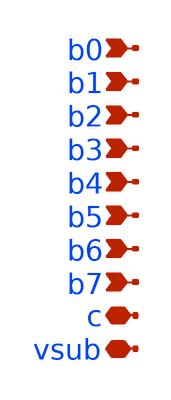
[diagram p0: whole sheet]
** sch_path: xschem/swcap_array_PEX.sch
**.subckt swcap_array_PEX b0 b1 b2 b3 b4 b5 b6 b7 c vsub
*.ipin b0
*.ipin b1
*.ipin b2
*.ipin b3
*.ipin b4
*.ipin b5
*.ipin b6
*.ipin b7
*.iopin c
*.iopin vsub
**** begin user architecture code

.subckt swcap_array C VSUB B0 B1 B2 B3 B4 B5 B6 B7

* NGSPICE file created from swcap_array_1.ext - technology: sky130A

X0 tcap_200f_60/a_173_157# C sky130_fd_pr__cap_mim_m3_2 l=1.6e+06u w=3.14e+07u
X1 tcap_200f_60/a_173_157# B7 VSUB VSUB sky130_fd_pr__nfet_01v8 ad=0p pd=0u as=0p ps=0u w=2e+06u
+ l=150000u
X3 tcap_200f_50/a_173_157# C sky130_fd_pr__cap_mim_m3_2 l=1.6e+06u w=3.14e+07u
X4 tcap_200f_50/a_173_157# B7 VSUB VSUB sky130_fd_pr__nfet_01v8 ad=0p pd=0u as=0p ps=0u w=2e+06u
+ l=150000u
X5 C tcap_200f_50/a_173_157# sky130_fd_pr__cap_mim_m3_1 l=1.6e+06u w=3.14e+07u
X6 tcap_200f_61/a_173_157# C sky130_fd_pr__cap_mim_m3_2 l=1.6e+06u w=3.14e+07u
X7 tcap_200f_61/a_173_157# B7 VSUB VSUB sky130_fd_pr__nfet_01v8 ad=0p pd=0u as=0p ps=0u w=2e+06u
+ l=150000u
X8 C tcap_200f_61/a_173_157# sky130_fd_pr__cap_mim_m3_1 l=1.6e+06u w=3.14e+07u
X9 tcap_200f_40/a_173_157# C sky130_fd_pr__cap_mim_m3_2 l=1.6e+06u w=3.14e+07u
X10 tcap_200f_40/a_173_157# B7 VSUB VSUB sky130_fd_pr__nfet_01v8 ad=0p pd=0u as=0p ps=0u w=2e+06u
+ l=150000u
X11 C tcap_200f_40/a_173_157# sky130_fd_pr__cap_mim_m3_1 l=1.6e+06u w=3.14e+07u
X12 tcap_200f_51/a_173_157# C sky130_fd_pr__cap_mim_m3_2 l=1.6e+06u w=3.14e+07u
X13 tcap_200f_51/a_173_157# B7 VSUB VSUB sky130_fd_pr__nfet_01v8 ad=0p pd=0u as=0p ps=0u w=2e+06u
+ l=150000u
X14 C tcap_200f_51/a_173_157# sky130_fd_pr__cap_mim_m3_1 l=1.6e+06u w=3.14e+07u
X15 tcap_200f_62/a_173_157# C sky130_fd_pr__cap_mim_m3_2 l=1.6e+06u w=3.14e+07u
X16 tcap_200f_62/a_173_157# B7 VSUB VSUB sky130_fd_pr__nfet_01v8 ad=0p pd=0u as=0p ps=0u w=2e+06u
+ l=150000u
X17 C tcap_200f_62/a_173_157# sky130_fd_pr__cap_mim_m3_1 l=1.6e+06u w=3.14e+07u
X18 tcap_200f_30/a_173_157# C sky130_fd_pr__cap_mim_m3_2 l=1.6e+06u w=3.14e+07u
X19 tcap_200f_30/a_173_157# B6 VSUB VSUB sky130_fd_pr__nfet_01v8 ad=0p pd=0u as=0p ps=0u w=2e+06u
+ l=150000u
X20 C tcap_200f_30/a_173_157# sky130_fd_pr__cap_mim_m3_1 l=1.6e+06u w=3.14e+07u
X21 tcap_200f_41/a_173_157# C sky130_fd_pr__cap_mim_m3_2 l=1.6e+06u w=3.14e+07u
X22 tcap_200f_41/a_173_157# B7 VSUB VSUB sky130_fd_pr__nfet_01v8 ad=0p pd=0u as=0p ps=0u w=2e+06u
+ l=150000u
X23 C tcap_200f_41/a_173_157# sky130_fd_pr__cap_mim_m3_1 l=1.6e+06u w=3.14e+07u
X24 tcap_200f_52/a_173_157# C sky130_fd_pr__cap_mim_m3_2 l=1.6e+06u w=3.14e+07u
X25 tcap_200f_52/a_173_157# B7 VSUB VSUB sky130_fd_pr__nfet_01v8 ad=0p pd=0u as=0p ps=0u w=2e+06u
+ l=150000u
X26 C tcap_200f_52/a_173_157# sky130_fd_pr__cap_mim_m3_1 l=1.6e+06u w=3.14e+07u
X27 tcap_200f_63/a_173_157# C sky130_fd_pr__cap_mim_m3_2 l=1.6e+06u w=3.14e+07u
X28 tcap_200f_63/a_173_157# B7 VSUB VSUB sky130_fd_pr__nfet_01v8 ad=0p pd=0u as=0p ps=0u w=2e+06u
+ l=150000u
X29 C tcap_200f_63/a_173_157# sky130_fd_pr__cap_mim_m3_1 l=1.6e+06u w=3.14e+07u
X30 tcap_50f_0/a_173_157# C sky130_fd_pr__cap_mim_m3_2 l=1.6e+06u w=7.85e+06u
X31 tcap_50f_0/a_173_157# B0 VSUB VSUB sky130_fd_pr__nfet_01v8 ad=0p pd=0u as=0p ps=0u w=2e+06u
+ l=150000u
X32 C tcap_50f_0/a_173_157# sky130_fd_pr__cap_mim_m3_1 l=1.6e+06u w=7.85e+06u
X33 tcap_200f_31/a_173_157# C sky130_fd_pr__cap_mim_m3_2 l=1.6e+06u w=3.14e+07u
X34 tcap_200f_31/a_173_157# B6 VSUB VSUB sky130_fd_pr__nfet_01v8 ad=0p pd=0u as=0p ps=0u w=2e+06u
+ l=150000u
X35 C tcap_200f_31/a_173_157# sky130_fd_pr__cap_mim_m3_1 l=1.6e+06u w=3.14e+07u
X36 tcap_200f_42/a_173_157# C sky130_fd_pr__cap_mim_m3_2 l=1.6e+06u w=3.14e+07u
X37 tcap_200f_42/a_173_157# B7 VSUB VSUB sky130_fd_pr__nfet_01v8 ad=0p pd=0u as=0p ps=0u w=2e+06u
+ l=150000u
X38 C tcap_200f_42/a_173_157# sky130_fd_pr__cap_mim_m3_1 l=1.6e+06u w=3.14e+07u
X39 tcap_200f_20/a_173_157# C sky130_fd_pr__cap_mim_m3_2 l=1.6e+06u w=3.14e+07u
X40 tcap_200f_20/a_173_157# B6 VSUB VSUB sky130_fd_pr__nfet_01v8 ad=0p pd=0u as=0p ps=0u w=2e+06u
+ l=150000u
X41 C tcap_200f_20/a_173_157# sky130_fd_pr__cap_mim_m3_1 l=1.6e+06u w=3.14e+07u
X42 tcap_200f_53/a_173_157# C sky130_fd_pr__cap_mim_m3_2 l=1.6e+06u w=3.14e+07u
X43 tcap_200f_53/a_173_157# B7 VSUB VSUB sky130_fd_pr__nfet_01v8 ad=0p pd=0u as=0p ps=0u w=2e+06u
+ l=150000u
X44 C tcap_200f_53/a_173_157# sky130_fd_pr__cap_mim_m3_1 l=1.6e+06u w=3.14e+07u
X45 tcap_200f_64/a_173_157# C sky130_fd_pr__cap_mim_m3_2 l=1.6e+06u w=3.14e+07u
X46 tcap_200f_64/a_173_157# B7 VSUB VSUB sky130_fd_pr__nfet_01v8 ad=0p pd=0u as=0p ps=0u w=2e+06u
+ l=150000u
X47 C tcap_200f_64/a_173_157# sky130_fd_pr__cap_mim_m3_1 l=1.6e+06u w=3.14e+07u
X48 tcap_200f_32/a_173_157# C sky130_fd_pr__cap_mim_m3_2 l=1.6e+06u w=3.14e+07u
X49 tcap_200f_32/a_173_157# B6 VSUB VSUB sky130_fd_pr__nfet_01v8 ad=0p pd=0u as=0p ps=0u w=2e+06u
+ l=150000u
X50 C tcap_200f_32/a_173_157# sky130_fd_pr__cap_mim_m3_1 l=1.6e+06u w=3.14e+07u
X51 tcap_200f_33/a_173_157# C sky130_fd_pr__cap_mim_m3_2 l=1.6e+06u w=3.14e+07u
X52 tcap_200f_33/a_173_157# B7 VSUB VSUB sky130_fd_pr__nfet_01v8 ad=0p pd=0u as=0p ps=0u w=2e+06u
+ l=150000u
X53 C tcap_200f_33/a_173_157# sky130_fd_pr__cap_mim_m3_1 l=1.6e+06u w=3.14e+07u
X54 tcap_200f_43/a_173_157# C sky130_fd_pr__cap_mim_m3_2 l=1.6e+06u w=3.14e+07u
X55 tcap_200f_43/a_173_157# B7 VSUB VSUB sky130_fd_pr__nfet_01v8 ad=0p pd=0u as=0p ps=0u w=2e+06u
+ l=150000u
X56 C tcap_200f_43/a_173_157# sky130_fd_pr__cap_mim_m3_1 l=1.6e+06u w=3.14e+07u
X57 tcap_200f_22/a_173_157# C sky130_fd_pr__cap_mim_m3_2 l=1.6e+06u w=3.14e+07u
X58 tcap_200f_22/a_173_157# B6 VSUB VSUB sky130_fd_pr__nfet_01v8 ad=0p pd=0u as=0p ps=0u w=2e+06u
+ l=150000u
X59 C tcap_200f_22/a_173_157# sky130_fd_pr__cap_mim_m3_1 l=1.6e+06u w=3.14e+07u
X60 tcap_200f_44/a_173_157# C sky130_fd_pr__cap_mim_m3_2 l=1.6e+06u w=3.14e+07u
X61 tcap_200f_44/a_173_157# B7 VSUB VSUB sky130_fd_pr__nfet_01v8 ad=0p pd=0u as=0p ps=0u w=2e+06u
+ l=150000u
X62 C tcap_200f_44/a_173_157# sky130_fd_pr__cap_mim_m3_1 l=1.6e+06u w=3.14e+07u
X63 tcap_200f_21/a_173_157# C sky130_fd_pr__cap_mim_m3_2 l=1.6e+06u w=3.14e+07u
X64 tcap_200f_21/a_173_157# B6 VSUB VSUB sky130_fd_pr__nfet_01v8 ad=0p pd=0u as=0p ps=0u w=2e+06u
+ l=150000u
X65 C tcap_200f_21/a_173_157# sky130_fd_pr__cap_mim_m3_1 l=1.6e+06u w=3.14e+07u
X66 tcap_200f_10/a_173_157# C sky130_fd_pr__cap_mim_m3_2 l=1.6e+06u w=3.14e+07u
X67 tcap_200f_10/a_173_157# B5 VSUB VSUB sky130_fd_pr__nfet_01v8 ad=0p pd=0u as=0p ps=0u w=2e+06u
+ l=150000u
X68 C tcap_200f_10/a_173_157# sky130_fd_pr__cap_mim_m3_1 l=1.6e+06u w=3.14e+07u
X69 tcap_200f_54/a_173_157# C sky130_fd_pr__cap_mim_m3_2 l=1.6e+06u w=3.14e+07u
X70 tcap_200f_54/a_173_157# B7 VSUB VSUB sky130_fd_pr__nfet_01v8 ad=0p pd=0u as=0p ps=0u w=2e+06u
+ l=150000u
X71 C tcap_200f_54/a_173_157# sky130_fd_pr__cap_mim_m3_1 l=1.6e+06u w=3.14e+07u
X72 tcap_200f_11/a_173_157# C sky130_fd_pr__cap_mim_m3_2 l=1.6e+06u w=3.14e+07u
X73 tcap_200f_11/a_173_157# B5 VSUB VSUB sky130_fd_pr__nfet_01v8 ad=0p pd=0u as=0p ps=0u w=2e+06u
+ l=150000u
X74 C tcap_200f_11/a_173_157# sky130_fd_pr__cap_mim_m3_1 l=1.6e+06u w=3.14e+07u
X75 tcap_200f_55/a_173_157# C sky130_fd_pr__cap_mim_m3_2 l=1.6e+06u w=3.14e+07u
X76 tcap_200f_55/a_173_157# B7 VSUB VSUB sky130_fd_pr__nfet_01v8 ad=0p pd=0u as=0p ps=0u w=2e+06u
+ l=150000u
X77 C tcap_200f_55/a_173_157# sky130_fd_pr__cap_mim_m3_1 l=1.6e+06u w=3.14e+07u
X78 tcap_200f_65/a_173_157# C sky130_fd_pr__cap_mim_m3_2 l=1.6e+06u w=3.14e+07u
X79 tcap_200f_65/a_173_157# B7 VSUB VSUB sky130_fd_pr__nfet_01v8 ad=0p pd=0u as=0p ps=0u w=2e+06u
+ l=150000u
X80 C tcap_200f_65/a_173_157# sky130_fd_pr__cap_mim_m3_1 l=1.6e+06u w=3.14e+07u
X81 tcap_200f_34/a_173_157# C sky130_fd_pr__cap_mim_m3_2 l=1.6e+06u w=3.14e+07u
X82 tcap_200f_34/a_173_157# B7 VSUB VSUB sky130_fd_pr__nfet_01v8 ad=0p pd=0u as=0p ps=0u w=2e+06u
+ l=150000u
X83 C tcap_200f_34/a_173_157# sky130_fd_pr__cap_mim_m3_1 l=1.6e+06u w=3.14e+07u
X84 tcap_200f_23/a_173_157# C sky130_fd_pr__cap_mim_m3_2 l=1.6e+06u w=3.14e+07u
X85 tcap_200f_23/a_173_157# B6 VSUB VSUB sky130_fd_pr__nfet_01v8 ad=0p pd=0u as=0p ps=0u w=2e+06u
+ l=150000u
X86 C tcap_200f_23/a_173_157# sky130_fd_pr__cap_mim_m3_1 l=1.6e+06u w=3.14e+07u
X87 tcap_200f_45/a_173_157# C sky130_fd_pr__cap_mim_m3_2 l=1.6e+06u w=3.14e+07u
X88 tcap_200f_45/a_173_157# B7 VSUB VSUB sky130_fd_pr__nfet_01v8 ad=0p pd=0u as=0p ps=0u w=2e+06u
+ l=150000u
X89 C tcap_200f_45/a_173_157# sky130_fd_pr__cap_mim_m3_1 l=1.6e+06u w=3.14e+07u
X90 tcap_200f_12/a_173_157# C sky130_fd_pr__cap_mim_m3_2 l=1.6e+06u w=3.14e+07u
X91 tcap_200f_12/a_173_157# B5 VSUB VSUB sky130_fd_pr__nfet_01v8 ad=0p pd=0u as=0p ps=0u w=2e+06u
+ l=150000u
X92 C tcap_200f_12/a_173_157# sky130_fd_pr__cap_mim_m3_1 l=1.6e+06u w=3.14e+07u
X93 tcap_200f_0/a_173_157# C sky130_fd_pr__cap_mim_m3_2 l=1.6e+06u w=3.14e+07u
X94 tcap_200f_0/a_173_157# B5 VSUB VSUB sky130_fd_pr__nfet_01v8 ad=0p pd=0u as=0p ps=0u w=2e+06u
+ l=150000u
X95 C tcap_200f_0/a_173_157# sky130_fd_pr__cap_mim_m3_1 l=1.6e+06u w=3.14e+07u
X96 tcap_200f_56/a_173_157# C sky130_fd_pr__cap_mim_m3_2 l=1.6e+06u w=3.14e+07u
X97 tcap_200f_56/a_173_157# B7 VSUB VSUB sky130_fd_pr__nfet_01v8 ad=0p pd=0u as=0p ps=0u w=2e+06u
+ l=150000u
X98 C tcap_200f_56/a_173_157# sky130_fd_pr__cap_mim_m3_1 l=1.6e+06u w=3.14e+07u
X99 tcap_200f_35/a_173_157# C sky130_fd_pr__cap_mim_m3_2 l=1.6e+06u w=3.14e+07u
X100 tcap_200f_35/a_173_157# B7 VSUB VSUB sky130_fd_pr__nfet_01v8 ad=0p pd=0u as=0p ps=0u w=2e+06u
+ l=150000u
X101 C tcap_200f_35/a_173_157# sky130_fd_pr__cap_mim_m3_1 l=1.6e+06u w=3.14e+07u
X102 tcap_200f_24/a_173_157# C sky130_fd_pr__cap_mim_m3_2 l=1.6e+06u w=3.14e+07u
X103 tcap_200f_24/a_173_157# B6 VSUB VSUB sky130_fd_pr__nfet_01v8 ad=0p pd=0u as=0p ps=0u w=2e+06u
+ l=150000u
X104 C tcap_200f_24/a_173_157# sky130_fd_pr__cap_mim_m3_1 l=1.6e+06u w=3.14e+07u
X105 tcap_200f_46/a_173_157# C sky130_fd_pr__cap_mim_m3_2 l=1.6e+06u w=3.14e+07u
X106 tcap_200f_46/a_173_157# B7 VSUB VSUB sky130_fd_pr__nfet_01v8 ad=0p pd=0u as=0p ps=0u w=2e+06u
+ l=150000u
X107 C tcap_200f_46/a_173_157# sky130_fd_pr__cap_mim_m3_1 l=1.6e+06u w=3.14e+07u
X108 tcap_200f_13/a_173_157# C sky130_fd_pr__cap_mim_m3_2 l=1.6e+06u w=3.14e+07u
X109 tcap_200f_13/a_173_157# B5 VSUB VSUB sky130_fd_pr__nfet_01v8 ad=0p pd=0u as=0p ps=0u w=2e+06u
+ l=150000u
X110 C tcap_200f_13/a_173_157# sky130_fd_pr__cap_mim_m3_1 l=1.6e+06u w=3.14e+07u
X111 tcap_200f_57/a_173_157# C sky130_fd_pr__cap_mim_m3_2 l=1.6e+06u w=3.14e+07u
X112 tcap_200f_57/a_173_157# B7 VSUB VSUB sky130_fd_pr__nfet_01v8 ad=0p pd=0u as=0p ps=0u w=2e+06u
+ l=150000u
X113 C tcap_200f_57/a_173_157# sky130_fd_pr__cap_mim_m3_1 l=1.6e+06u w=3.14e+07u
X114 tcap_200f_36/a_173_157# C sky130_fd_pr__cap_mim_m3_2 l=1.6e+06u w=3.14e+07u
X115 tcap_200f_36/a_173_157# B7 VSUB VSUB sky130_fd_pr__nfet_01v8 ad=0p pd=0u as=0p ps=0u w=2e+06u
+ l=150000u
X116 C tcap_200f_36/a_173_157# sky130_fd_pr__cap_mim_m3_1 l=1.6e+06u w=3.14e+07u
X117 tcap_200f_25/a_173_157# C sky130_fd_pr__cap_mim_m3_2 l=1.6e+06u w=3.14e+07u
X118 tcap_200f_25/a_173_157# B6 VSUB VSUB sky130_fd_pr__nfet_01v8 ad=0p pd=0u as=0p ps=0u w=2e+06u
+ l=150000u
X119 C tcap_200f_25/a_173_157# sky130_fd_pr__cap_mim_m3_1 l=1.6e+06u w=3.14e+07u
X120 tcap_200f_47/a_173_157# C sky130_fd_pr__cap_mim_m3_2 l=1.6e+06u w=3.14e+07u
X121 tcap_200f_47/a_173_157# B7 VSUB VSUB sky130_fd_pr__nfet_01v8 ad=0p pd=0u as=0p ps=0u w=2e+06u
+ l=150000u
X122 C tcap_200f_47/a_173_157# sky130_fd_pr__cap_mim_m3_1 l=1.6e+06u w=3.14e+07u
X123 tcap_200f_14/a_173_157# C sky130_fd_pr__cap_mim_m3_2 l=1.6e+06u w=3.14e+07u
X124 tcap_200f_14/a_173_157# B5 VSUB VSUB sky130_fd_pr__nfet_01v8 ad=0p pd=0u as=0p ps=0u w=2e+06u
+ l=150000u
X125 C tcap_200f_14/a_173_157# sky130_fd_pr__cap_mim_m3_1 l=1.6e+06u w=3.14e+07u
X126 tcap_200f_58/a_173_157# C sky130_fd_pr__cap_mim_m3_2 l=1.6e+06u w=3.14e+07u
X127 tcap_200f_58/a_173_157# B7 VSUB VSUB sky130_fd_pr__nfet_01v8 ad=0p pd=0u as=0p ps=0u w=2e+06u
+ l=150000u
X128 C tcap_200f_58/a_173_157# sky130_fd_pr__cap_mim_m3_1 l=1.6e+06u w=3.14e+07u
X129 tcap_200f_37/a_173_157# C sky130_fd_pr__cap_mim_m3_2 l=1.6e+06u w=3.14e+07u
X130 tcap_200f_37/a_173_157# B7 VSUB VSUB sky130_fd_pr__nfet_01v8 ad=0p pd=0u as=0p ps=0u w=2e+06u
+ l=150000u
X131 C tcap_200f_37/a_173_157# sky130_fd_pr__cap_mim_m3_1 l=1.6e+06u w=3.14e+07u
X132 tcap_200f_26/a_173_157# C sky130_fd_pr__cap_mim_m3_2 l=1.6e+06u w=3.14e+07u
X133 tcap_200f_26/a_173_157# B6 VSUB VSUB sky130_fd_pr__nfet_01v8 ad=0p pd=0u as=0p ps=0u w=2e+06u
+ l=150000u
X134 C tcap_200f_26/a_173_157# sky130_fd_pr__cap_mim_m3_1 l=1.6e+06u w=3.14e+07u
X135 tcap_200f_15/a_173_157# C sky130_fd_pr__cap_mim_m3_2 l=1.6e+06u w=3.14e+07u
X136 tcap_200f_15/a_173_157# B6 VSUB VSUB sky130_fd_pr__nfet_01v8 ad=0p pd=0u as=0p ps=0u w=2e+06u
+ l=150000u
X137 C tcap_200f_15/a_173_157# sky130_fd_pr__cap_mim_m3_1 l=1.6e+06u w=3.14e+07u
X138 tcap_200f_48/a_173_157# C sky130_fd_pr__cap_mim_m3_2 l=1.6e+06u w=3.14e+07u
X139 tcap_200f_48/a_173_157# B7 VSUB VSUB sky130_fd_pr__nfet_01v8 ad=0p pd=0u as=0p ps=0u w=2e+06u
+ l=150000u
X140 C tcap_200f_48/a_173_157# sky130_fd_pr__cap_mim_m3_1 l=1.6e+06u w=3.14e+07u
X141 tcap_200f_59/a_173_157# C sky130_fd_pr__cap_mim_m3_2 l=1.6e+06u w=3.14e+07u
X142 tcap_200f_59/a_173_157# B7 VSUB VSUB sky130_fd_pr__nfet_01v8 ad=0p pd=0u as=0p ps=0u w=2e+06u
+ l=150000u
X143 C tcap_200f_59/a_173_157# sky130_fd_pr__cap_mim_m3_1 l=1.6e+06u w=3.14e+07u
X144 tcap_200f_3/a_173_157# C sky130_fd_pr__cap_mim_m3_2 l=1.6e+06u w=3.14e+07u
X145 tcap_200f_3/a_173_157# B2 VSUB VSUB sky130_fd_pr__nfet_01v8 ad=0p pd=0u as=0p ps=0u w=2e+06u
+ l=150000u
X146 C tcap_200f_3/a_173_157# sky130_fd_pr__cap_mim_m3_1 l=1.6e+06u w=3.14e+07u
X147 tcap_200f_38/a_173_157# C sky130_fd_pr__cap_mim_m3_2 l=1.6e+06u w=3.14e+07u
X148 tcap_200f_38/a_173_157# B7 VSUB VSUB sky130_fd_pr__nfet_01v8 ad=0p pd=0u as=0p ps=0u w=2e+06u
+ l=150000u
X149 C tcap_200f_38/a_173_157# sky130_fd_pr__cap_mim_m3_1 l=1.6e+06u w=3.14e+07u
X150 tcap_200f_27/a_173_157# C sky130_fd_pr__cap_mim_m3_2 l=1.6e+06u w=3.14e+07u
X151 tcap_200f_27/a_173_157# B6 VSUB VSUB sky130_fd_pr__nfet_01v8 ad=0p pd=0u as=0p ps=0u w=2e+06u
+ l=150000u
X152 C tcap_200f_27/a_173_157# sky130_fd_pr__cap_mim_m3_1 l=1.6e+06u w=3.14e+07u
X153 tcap_200f_16/a_173_157# C sky130_fd_pr__cap_mim_m3_2 l=1.6e+06u w=3.14e+07u
X154 tcap_200f_16/a_173_157# B5 VSUB VSUB sky130_fd_pr__nfet_01v8 ad=0p pd=0u as=0p ps=0u w=2e+06u
+ l=150000u
X155 C tcap_200f_16/a_173_157# sky130_fd_pr__cap_mim_m3_1 l=1.6e+06u w=3.14e+07u
X156 tcap_200f_49/a_173_157# C sky130_fd_pr__cap_mim_m3_2 l=1.6e+06u w=3.14e+07u
X157 tcap_200f_49/a_173_157# B7 VSUB VSUB sky130_fd_pr__nfet_01v8 ad=0p pd=0u as=0p ps=0u w=2e+06u
+ l=150000u
X158 C tcap_200f_49/a_173_157# sky130_fd_pr__cap_mim_m3_1 l=1.6e+06u w=3.14e+07u
X159 tcap_200f_4/a_173_157# C sky130_fd_pr__cap_mim_m3_2 l=1.6e+06u w=3.14e+07u
X160 tcap_200f_4/a_173_157# B3 VSUB VSUB sky130_fd_pr__nfet_01v8 ad=0p pd=0u as=0p ps=0u w=2e+06u
+ l=150000u
X161 C tcap_200f_4/a_173_157# sky130_fd_pr__cap_mim_m3_1 l=1.6e+06u w=3.14e+07u
X162 tcap_200f_28/a_173_157# C sky130_fd_pr__cap_mim_m3_2 l=1.6e+06u w=3.14e+07u
X163 tcap_200f_28/a_173_157# B6 VSUB VSUB sky130_fd_pr__nfet_01v8 ad=0p pd=0u as=0p ps=0u w=2e+06u
+ l=150000u
X164 C tcap_200f_28/a_173_157# sky130_fd_pr__cap_mim_m3_1 l=1.6e+06u w=3.14e+07u
X165 tcap_200f_39/a_173_157# C sky130_fd_pr__cap_mim_m3_2 l=1.6e+06u w=3.14e+07u
X166 tcap_200f_39/a_173_157# B7 VSUB VSUB sky130_fd_pr__nfet_01v8 ad=0p pd=0u as=0p ps=0u w=2e+06u
+ l=150000u
X167 C tcap_200f_39/a_173_157# sky130_fd_pr__cap_mim_m3_1 l=1.6e+06u w=3.14e+07u
X168 tcap_200f_17/a_173_157# C sky130_fd_pr__cap_mim_m3_2 l=1.6e+06u w=3.14e+07u
X169 tcap_200f_17/a_173_157# B5 VSUB VSUB sky130_fd_pr__nfet_01v8 ad=0p pd=0u as=0p ps=0u w=2e+06u
+ l=150000u
X170 C tcap_200f_17/a_173_157# sky130_fd_pr__cap_mim_m3_1 l=1.6e+06u w=3.14e+07u
X171 tcap_200f_5/a_173_157# C sky130_fd_pr__cap_mim_m3_2 l=1.6e+06u w=3.14e+07u
X172 tcap_200f_5/a_173_157# B3 VSUB VSUB sky130_fd_pr__nfet_01v8 ad=0p pd=0u as=0p ps=0u w=2e+06u
+ l=150000u
X173 C tcap_200f_5/a_173_157# sky130_fd_pr__cap_mim_m3_1 l=1.6e+06u w=3.14e+07u
X174 tcap_200f_29/a_173_157# C sky130_fd_pr__cap_mim_m3_2 l=1.6e+06u w=3.14e+07u
X175 tcap_200f_29/a_173_157# B6 VSUB VSUB sky130_fd_pr__nfet_01v8 ad=0p pd=0u as=0p ps=0u w=2e+06u
+ l=150000u
X176 C tcap_200f_29/a_173_157# sky130_fd_pr__cap_mim_m3_1 l=1.6e+06u w=3.14e+07u
X177 tcap_200f_18/a_173_157# C sky130_fd_pr__cap_mim_m3_2 l=1.6e+06u w=3.14e+07u
X178 tcap_200f_18/a_173_157# B6 VSUB VSUB sky130_fd_pr__nfet_01v8 ad=0p pd=0u as=0p ps=0u w=2e+06u
+ l=150000u
X179 C tcap_200f_18/a_173_157# sky130_fd_pr__cap_mim_m3_1 l=1.6e+06u w=3.14e+07u
X180 tcap_200f_6/a_173_157# C sky130_fd_pr__cap_mim_m3_2 l=1.6e+06u w=3.14e+07u
X181 tcap_200f_6/a_173_157# B4 VSUB VSUB sky130_fd_pr__nfet_01v8 ad=0p pd=0u as=0p ps=0u w=2e+06u
+ l=150000u
X182 C tcap_200f_6/a_173_157# sky130_fd_pr__cap_mim_m3_1 l=1.6e+06u w=3.14e+07u
X183 tcap_200f_19/a_173_157# C sky130_fd_pr__cap_mim_m3_2 l=1.6e+06u w=3.14e+07u
X184 tcap_200f_19/a_173_157# B6 VSUB VSUB sky130_fd_pr__nfet_01v8 ad=0p pd=0u as=0p ps=0u w=2e+06u
+ l=150000u
X185 C tcap_200f_19/a_173_157# sky130_fd_pr__cap_mim_m3_1 l=1.6e+06u w=3.14e+07u
X186 tcap_200f_8/a_173_157# C sky130_fd_pr__cap_mim_m3_2 l=1.6e+06u w=3.14e+07u
X187 tcap_200f_8/a_173_157# B4 VSUB VSUB sky130_fd_pr__nfet_01v8 ad=0p pd=0u as=0p ps=0u w=2e+06u
+ l=150000u
X188 C tcap_200f_8/a_173_157# sky130_fd_pr__cap_mim_m3_1 l=1.6e+06u w=3.14e+07u
X189 tcap_200f_7/a_173_157# C sky130_fd_pr__cap_mim_m3_2 l=1.6e+06u w=3.14e+07u
X190 tcap_200f_7/a_173_157# B4 VSUB VSUB sky130_fd_pr__nfet_01v8 ad=0p pd=0u as=0p ps=0u w=2e+06u
+ l=150000u
X191 C tcap_200f_7/a_173_157# sky130_fd_pr__cap_mim_m3_1 l=1.6e+06u w=3.14e+07u
X192 tcap_200f_9/a_173_157# C sky130_fd_pr__cap_mim_m3_2 l=1.6e+06u w=3.14e+07u
X193 tcap_200f_9/a_173_157# B4 VSUB VSUB sky130_fd_pr__nfet_01v8 ad=0p pd=0u as=0p ps=0u w=2e+06u
+ l=150000u
X194 C tcap_200f_9/a_173_157# sky130_fd_pr__cap_mim_m3_1 l=1.6e+06u w=3.14e+07u
X195 tcap_100f_0/a_173_157# C sky130_fd_pr__cap_mim_m3_2 l=1.6e+06u w=1.57e+07u
X196 tcap_100f_0/a_173_157# B1 VSUB VSUB sky130_fd_pr__nfet_01v8 ad=0p pd=0u as=0p ps=0u w=2e+06u
+ l=150000u
X197 C tcap_100f_0/a_173_157# sky130_fd_pr__cap_mim_m3_1 l=1.6e+06u w=1.57e+07u
C0 C tcap_100f_0/a_173_157# 5.85fF
C1 tcap_200f_36/a_173_157# tcap_200f_37/a_173_157# 4.48fF
C2 tcap_200f_38/a_173_157# tcap_200f_37/a_173_157# 4.48fF
C3 tcap_200f_28/a_173_157# tcap_200f_31/a_173_157# 4.47fF
C4 tcap_200f_10/a_173_157# tcap_200f_13/a_173_157# 4.47fF
C5 tcap_200f_45/a_173_157# C 12.05fF
C6 tcap_200f_44/a_173_157# C 12.05fF
C7 tcap_200f_16/a_173_157# tcap_200f_14/a_173_157# 4.47fF
C8 C tcap_200f_52/a_173_157# 12.05fF
C9 tcap_200f_57/a_173_157# tcap_200f_58/a_173_157# 4.48fF
C10 tcap_200f_17/a_173_157# tcap_200f_16/a_173_157# 4.47fF
C11 tcap_200f_18/a_173_157# C 12.05fF
C12 tcap_200f_12/a_173_157# C 12.05fF
C13 tcap_200f_47/a_173_157# tcap_200f_46/a_173_157# 4.48fF
C14 tcap_200f_49/a_173_157# tcap_200f_50/a_173_157# 4.48fF
C15 tcap_200f_56/a_173_157# C 12.05fF
C16 tcap_200f_54/a_173_157# tcap_200f_53/a_173_157# 4.48fF
C17 tcap_200f_41/a_173_157# tcap_200f_40/a_173_157# 4.48fF
C18 tcap_200f_15/a_173_157# C 12.05fF
C19 C tcap_200f_7/a_173_157# 12.05fF
C20 tcap_200f_15/a_173_157# tcap_200f_25/a_173_157# 4.47fF
C21 tcap_200f_36/a_173_157# C 12.05fF
C22 tcap_200f_38/a_173_157# C 12.05fF
C23 tcap_200f_5/a_173_157# C 12.05fF
C24 tcap_200f_22/a_173_157# C 12.05fF
C25 tcap_200f_42/a_173_157# C 12.05fF
C26 tcap_200f_48/a_173_157# tcap_200f_47/a_173_157# 4.48fF
C27 tcap_200f_34/a_173_157# C 11.79fF
C28 tcap_200f_52/a_173_157# tcap_200f_53/a_173_157# 4.48fF
C29 C tcap_200f_6/a_173_157# 12.05fF
C30 tcap_200f_44/a_173_157# tcap_200f_43/a_173_157# 4.48fF
C31 tcap_200f_31/a_173_157# tcap_200f_30/a_173_157# 4.47fF
C32 tcap_200f_36/a_173_157# tcap_200f_35/a_173_157# 4.48fF
C33 tcap_200f_39/a_173_157# C 12.05fF
C34 tcap_200f_45/a_173_157# tcap_200f_46/a_173_157# 4.48fF
C35 tcap_200f_4/a_173_157# tcap_200f_3/a_173_157# 4.47fF
C36 tcap_200f_16/a_173_157# C 12.05fF
C37 tcap_200f_59/a_173_157# C 12.05fF
C38 tcap_200f_14/a_173_157# C 12.05fF
C39 tcap_200f_23/a_173_157# tcap_200f_22/a_173_157# 4.47fF
C40 tcap_200f_34/a_173_157# tcap_200f_35/a_173_157# 4.48fF
C41 tcap_200f_61/a_173_157# tcap_200f_62/a_173_157# 4.48fF
C42 tcap_200f_55/a_173_157# tcap_200f_54/a_173_157# 4.48fF
C43 C tcap_200f_37/a_173_157# 12.05fF
C44 tcap_200f_15/a_173_157# tcap_200f_27/a_173_157# 4.47fF
C45 tcap_200f_51/a_173_157# tcap_200f_50/a_173_157# 4.48fF
C46 tcap_200f_63/a_173_157# tcap_200f_62/a_173_157# 4.48fF
C47 tcap_200f_57/a_173_157# tcap_200f_56/a_173_157# 4.48fF
C48 tcap_200f_17/a_173_157# C 12.05fF
C49 tcap_200f_11/a_173_157# tcap_200f_0/a_173_157# 4.47fF
C50 tcap_50f_0/a_173_157# C 3.01fF
C51 tcap_200f_8/a_173_157# tcap_200f_7/a_173_157# 4.47fF
C52 tcap_200f_11/a_173_157# C 12.05fF
C53 tcap_200f_42/a_173_157# tcap_200f_43/a_173_157# 4.48fF
C54 tcap_200f_60/a_173_157# tcap_200f_61/a_173_157# 4.48fF
C55 tcap_200f_3/a_173_157# tcap_100f_0/a_173_157# 2.53fF
C56 tcap_200f_21/a_173_157# tcap_200f_22/a_173_157# 4.47fF
C57 tcap_200f_0/a_173_157# C 12.05fF
C58 tcap_200f_24/a_173_157# C 12.05fF
C59 tcap_200f_52/a_173_157# tcap_200f_51/a_173_157# 4.48fF
C60 tcap_200f_55/a_173_157# tcap_200f_56/a_173_157# 4.48fF
C61 tcap_200f_24/a_173_157# tcap_200f_25/a_173_157# 4.47fF
C62 tcap_200f_64/a_173_157# C 11.71fF
C63 tcap_200f_29/a_173_157# C 12.05fF
C64 B4 B5 3.35fF
C65 tcap_200f_20/a_173_157# C 12.05fF
C66 tcap_200f_42/a_173_157# tcap_200f_41/a_173_157# 4.48fF
C67 tcap_200f_25/a_173_157# C 12.05fF
C68 tcap_200f_18/a_173_157# tcap_200f_19/a_173_157# 4.47fF
C69 tcap_200f_23/a_173_157# tcap_200f_24/a_173_157# 4.47fF
C70 tcap_200f_10/a_173_157# tcap_200f_11/a_173_157# 4.47fF
C71 tcap_200f_12/a_173_157# tcap_200f_13/a_173_157# 4.47fF
C72 C tcap_200f_35/a_173_157# 12.05fF
C73 tcap_200f_5/a_173_157# tcap_200f_4/a_173_157# 4.47fF
C74 B5 B6 6.53fF
C75 tcap_200f_29/a_173_157# tcap_200f_28/a_173_157# 4.47fF
C76 tcap_200f_23/a_173_157# C 12.05fF
C77 tcap_200f_26/a_173_157# tcap_200f_29/a_173_157# 4.47fF
C78 tcap_200f_28/a_173_157# C 12.05fF
C79 tcap_200f_44/a_173_157# tcap_200f_45/a_173_157# 4.48fF
C80 tcap_200f_26/a_173_157# C 12.05fF
C81 tcap_200f_9/a_173_157# tcap_200f_0/a_173_157# 4.47fF
C82 tcap_200f_32/a_173_157# C 11.60fF
C83 tcap_200f_10/a_173_157# C 12.05fF
C84 tcap_200f_27/a_173_157# C 12.05fF
C85 tcap_200f_39/a_173_157# tcap_200f_40/a_173_157# 4.48fF
C86 tcap_200f_34/a_173_157# tcap_200f_33/a_173_157# 4.48fF
C87 C tcap_200f_53/a_173_157# 12.05fF
C88 tcap_200f_57/a_173_157# C 12.05fF
C89 tcap_200f_43/a_173_157# C 12.05fF
C90 tcap_200f_9/a_173_157# C 12.05fF
C91 tcap_200f_49/a_173_157# C 12.05fF
C92 C tcap_200f_8/a_173_157# 12.05fF
C93 C tcap_200f_46/a_173_157# 12.05fF
C94 tcap_200f_21/a_173_157# C 12.05fF
C95 tcap_200f_21/a_173_157# tcap_200f_20/a_173_157# 4.47fF
C96 tcap_200f_59/a_173_157# tcap_200f_58/a_173_157# 4.48fF
C97 tcap_200f_64/a_173_157# tcap_200f_65/a_173_157# 4.48fF
C98 C tcap_200f_65/a_173_157# 10.91fF
C99 tcap_200f_41/a_173_157# C 12.05fF
C100 tcap_200f_26/a_173_157# tcap_200f_27/a_173_157# 4.47fF
C101 tcap_200f_48/a_173_157# C 12.05fF
C102 tcap_200f_55/a_173_157# C 12.05fF
C103 tcap_200f_59/a_173_157# tcap_200f_60/a_173_157# 4.48fF
C104 C tcap_200f_30/a_173_157# 11.79fF
C105 tcap_200f_4/a_173_157# C 11.89fF
C106 B7 B6 9.55fF
C107 C tcap_200f_62/a_173_157# 12.05fF
C108 C tcap_200f_51/a_173_157# 12.05fF
C109 tcap_200f_19/a_173_157# C 12.05fF
C110 tcap_200f_19/a_173_157# tcap_200f_20/a_173_157# 4.47fF
C111 tcap_200f_9/a_173_157# tcap_200f_8/a_173_157# 4.47fF
C112 C tcap_200f_40/a_173_157# 12.05fF
C113 C tcap_200f_13/a_173_157# 12.05fF
C114 tcap_200f_6/a_173_157# tcap_200f_7/a_173_157# 4.47fF
C115 C tcap_200f_3/a_173_157# 11.41fF
C116 tcap_200f_33/a_173_157# C 11.60fF
C117 tcap_200f_61/a_173_157# C 12.05fF
C118 tcap_200f_14/a_173_157# tcap_200f_12/a_173_157# 4.47fF
C119 tcap_200f_47/a_173_157# C 12.05fF
C120 tcap_200f_58/a_173_157# C 12.05fF
C121 C tcap_200f_31/a_173_157# 12.05fF
C122 tcap_200f_64/a_173_157# tcap_200f_63/a_173_157# 4.48fF
C123 tcap_200f_5/a_173_157# tcap_200f_6/a_173_157# 4.47fF
C124 tcap_200f_32/a_173_157# tcap_200f_30/a_173_157# 4.47fF
C125 C tcap_200f_50/a_173_157# 12.05fF
C126 tcap_200f_39/a_173_157# tcap_200f_38/a_173_157# 4.48fF
C127 C tcap_200f_63/a_173_157# 12.04fF
C128 tcap_200f_18/a_173_157# tcap_200f_17/a_173_157# 4.47fF
C129 tcap_200f_48/a_173_157# tcap_200f_49/a_173_157# 4.48fF
C130 tcap_200f_60/a_173_157# C 12.05fF
C131 tcap_200f_54/a_173_157# C 12.05fF
C132 tcap_100f_0/a_173_157# VSUB 4.99fF $ **FLOATING
C133 tcap_200f_9/a_173_157# VSUB 7.94fF $ **FLOATING
C134 tcap_200f_7/a_173_157# VSUB 7.94fF $ **FLOATING
C135 tcap_200f_8/a_173_157# VSUB 7.94fF $ **FLOATING
C136 tcap_200f_19/a_173_157# VSUB 7.94fF $ **FLOATING
C137 tcap_200f_6/a_173_157# VSUB 7.94fF $ **FLOATING
C138 B4 VSUB 5.01fF $ **FLOATING
C139 tcap_200f_18/a_173_157# VSUB 7.94fF $ **FLOATING
C140 B6 VSUB 22.15fF $ **FLOATING
C141 tcap_200f_29/a_173_157# VSUB 7.94fF $ **FLOATING
C142 tcap_200f_5/a_173_157# VSUB 7.94fF $ **FLOATING
C143 tcap_200f_17/a_173_157# VSUB 7.94fF $ **FLOATING
C144 tcap_200f_39/a_173_157# VSUB 7.96fF $ **FLOATING
C145 tcap_200f_28/a_173_157# VSUB 7.94fF $ **FLOATING
C146 tcap_200f_4/a_173_157# VSUB 7.94fF $ **FLOATING
C147 B3 VSUB 2.41fF $ **FLOATING
C148 tcap_200f_49/a_173_157# VSUB 7.96fF $ **FLOATING
C149 tcap_200f_16/a_173_157# VSUB 7.94fF $ **FLOATING
C150 tcap_200f_27/a_173_157# VSUB 7.94fF $ **FLOATING
C151 tcap_200f_38/a_173_157# VSUB 7.96fF $ **FLOATING
C152 tcap_200f_3/a_173_157# VSUB 7.94fF $ **FLOATING
C153 tcap_200f_59/a_173_157# VSUB 7.95fF $ **FLOATING
C154 tcap_200f_48/a_173_157# VSUB 7.96fF $ **FLOATING
C155 tcap_200f_15/a_173_157# VSUB 7.94fF $ **FLOATING
C156 tcap_200f_26/a_173_157# VSUB 7.94fF $ **FLOATING
C157 tcap_200f_37/a_173_157# VSUB 7.96fF $ **FLOATING
C158 tcap_200f_58/a_173_157# VSUB 7.95fF $ **FLOATING
C159 tcap_200f_14/a_173_157# VSUB 7.94fF $ **FLOATING
C160 tcap_200f_47/a_173_157# VSUB 7.96fF $ **FLOATING
C161 tcap_200f_25/a_173_157# VSUB 7.94fF $ **FLOATING
C162 tcap_200f_36/a_173_157# VSUB 7.96fF $ **FLOATING
C163 tcap_200f_57/a_173_157# VSUB 7.95fF $ **FLOATING
C164 tcap_200f_13/a_173_157# VSUB 7.94fF $ **FLOATING
C165 tcap_200f_46/a_173_157# VSUB 7.96fF $ **FLOATING
C166 tcap_200f_24/a_173_157# VSUB 7.94fF $ **FLOATING
C167 tcap_200f_35/a_173_157# VSUB 7.96fF $ **FLOATING
C168 tcap_200f_56/a_173_157# VSUB 7.95fF $ **FLOATING
C169 tcap_200f_0/a_173_157# VSUB 7.94fF $ **FLOATING
C170 B5 VSUB 10.51fF $ **FLOATING
C171 tcap_200f_12/a_173_157# VSUB 7.94fF $ **FLOATING
C172 tcap_200f_45/a_173_157# VSUB 7.96fF $ **FLOATING
C173 tcap_200f_23/a_173_157# VSUB 7.94fF $ **FLOATING
C174 tcap_200f_34/a_173_157# VSUB 7.95fF $ **FLOATING
C175 C VSUB 71.74fF $ **FLOATING
C176 tcap_200f_65/a_173_157# VSUB 7.92fF $ **FLOATING
C177 B7 VSUB 28.92fF $ **FLOATING
C178 tcap_200f_55/a_173_157# VSUB 7.95fF $ **FLOATING
C179 tcap_200f_11/a_173_157# VSUB 7.94fF $ **FLOATING
C180 tcap_200f_54/a_173_157# VSUB 7.95fF $ **FLOATING
C181 tcap_200f_10/a_173_157# VSUB 7.94fF $ **FLOATING
C182 tcap_200f_21/a_173_157# VSUB 7.94fF $ **FLOATING
C183 tcap_200f_44/a_173_157# VSUB 7.96fF $ **FLOATING
C184 tcap_200f_22/a_173_157# VSUB 7.94fF $ **FLOATING
C185 tcap_200f_43/a_173_157# VSUB 7.96fF $ **FLOATING
C186 tcap_200f_33/a_173_157# VSUB 7.96fF $ **FLOATING
C187 tcap_200f_32/a_173_157# VSUB 7.96fF $ **FLOATING
C188 tcap_200f_64/a_173_157# VSUB 7.93fF $ **FLOATING
C189 tcap_200f_53/a_173_157# VSUB 7.95fF $ **FLOATING
C190 tcap_200f_20/a_173_157# VSUB 7.94fF $ **FLOATING
C191 tcap_200f_42/a_173_157# VSUB 7.96fF $ **FLOATING
C192 tcap_200f_31/a_173_157# VSUB 7.94fF $ **FLOATING
C193 tcap_50f_0/a_173_157# VSUB 3.60fF $ **FLOATING
C194 tcap_200f_63/a_173_157# VSUB 7.94fF $ **FLOATING
C195 tcap_200f_52/a_173_157# VSUB 7.95fF $ **FLOATING
C196 tcap_200f_41/a_173_157# VSUB 7.96fF $ **FLOATING
C197 tcap_200f_30/a_173_157# VSUB 7.94fF $ **FLOATING
C198 tcap_200f_62/a_173_157# VSUB 7.94fF $ **FLOATING
C199 tcap_200f_51/a_173_157# VSUB 7.95fF $ **FLOATING
C200 tcap_200f_40/a_173_157# VSUB 7.96fF $ **FLOATING
C201 tcap_200f_61/a_173_157# VSUB 7.95fF $ **FLOATING
C202 tcap_200f_50/a_173_157# VSUB 7.95fF $ **FLOATING
C203 tcap_200f_60/a_173_157# VSUB 7.95fF $ **FLOATING



.ends
XDUT c vsub b0 b1 b2 b3 b4 b5 b6 b7 swcap_array



**** end user architecture code
**.ends
.end
